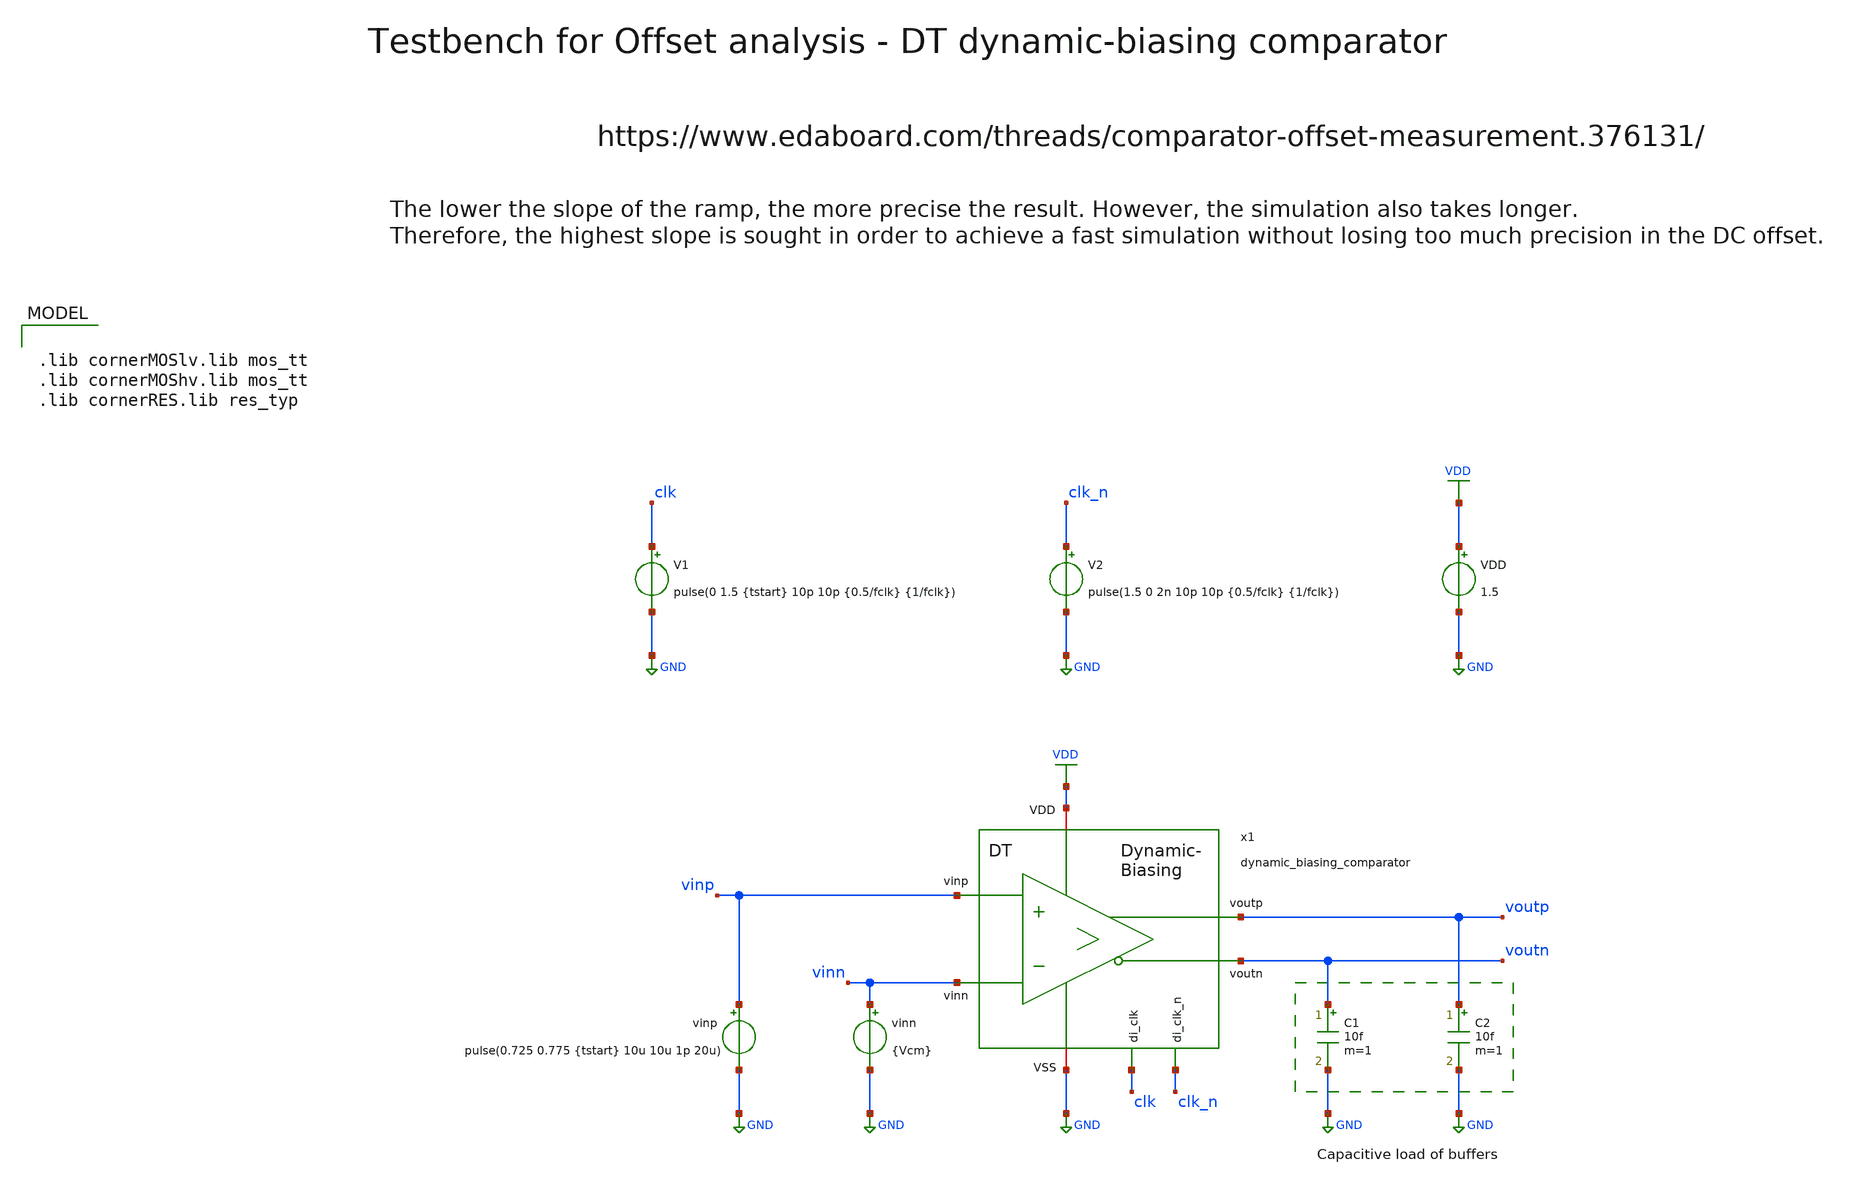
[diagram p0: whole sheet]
** sch_path: SG13G2_ATBS-ADC-main/xschem/comparator/discrete_time/Dynamic-biasing/testbenches/dynamic_biasing_comparator_tb_tran_offset.sch
**.subckt dynamic_biasing_comparator_tb_tran_offset
VDD VDD GND 1.5
V1 clk GND pulse(0 1.5 {tstart} 10p 10p {0.5/fclk} {1/fclk})
vinn vinn GND {Vcm}
vinp vinp GND pulse(0.725 0.775 {tstart} 10u 10u 1p 20u)
V2 clk_n GND pulse(1.5 0 2n 10p 10p {0.5/fclk} {1/fclk})
C1 voutn GND 10f m=1
C2 voutp GND 10f m=1
x1 clk_n clk VDD voutp vinp GND voutn vinn dynamic_biasing_comparator
**** begin user architecture code

.lib cornerMOSlv.lib mos_tt
.lib cornerMOShv.lib mos_tt
.lib cornerRES.lib res_typ



.param temp=27
.param fclk=8000000
.param tstart=2n
.param Vcm=0.75
.csparam fclk=fclk
.csparam tstart=tstart
.csparam Vcm=Vcm
.options klu method=gear reltol=1e-3 abstol=1e-12 gmin=1e-15
.control
* save all

* User Constants
let tstop = 20u
let tstep = 1/fclk

* Operating Point Analysis
op
remzerovec
write dynamic_biasing_comparator_tb_tran_offset.raw
set appendwrite

* Transient Analysis
tran $&tstep $&tstop
write dynamic_biasing_comparator_tb_tran_offset.raw

* Measure offset increasing ramp
let voutp_limit = 0.9 * 1.5
meas tran tcross WHEN v(voutp)=voutp_limit RISE=1
print tcross
meas tran vinp_voff FIND v(vinp) at=tcross
let voff_inc = vinp_voff - Vcm
print voff_inc

* Measure offset decreasing ramp
let voutn_limit = 0.9 * 1.5
let tmiddle = tstop/2
meas tran tcross WHEN v(voutn)=voutn_limit from=tmiddle RISE=1
print tcross
meas tran vinp_voff FIND v(vinp) at=tcross
let voff_dec = vinp_voff - Vcm
print voff_dec

* Plotting
plot v(clk) v(voutp) v(voutn) v(vinp) v(vinn)

* Writing Data
set wr_singlescale
set wr_vecnames
wrdata
+ /foss/designs/SG13G2_ATBS-ADC-main/python/plot_simulations/data/dynamic_biasing_comparator_tb_tran_offset.txt v(clk) v(voutp) v(voutn) v(vinp) v(vinn)

*quit
.endc

**** end user architecture code
**.ends

* expanding   symbol:  comparator/discrete_time/Dynamic-biasing/dynamic_biasing_comparator.sym # of
*+ pins=8
** sym_path: SG13G2_ATBS-ADC-main/xschem/comparator/discrete_time/Dynamic-biasing/dynamic_biasing_comparator.sym
** sch_path: SG13G2_ATBS-ADC-main/xschem/comparator/discrete_time/Dynamic-biasing/dynamic_biasing_comparator.sch
.subckt dynamic_biasing_comparator di_clk_n di_clk VDD voutp vinp VSS voutn vinn
*.iopin VDD
*.opin voutp
*.opin voutn
*.ipin di_clk_n
*.iopin VSS
*.ipin vinp
*.ipin vinn
*.ipin di_clk
XM3a vs di_clk vctail VSS sg13_lv_nmos w=1.0u l=0.13u ng=1 m=1 mm_ok=1
XM12 voutp di_clk_n VSS VSS sg13_lv_nmos w=1.0u l=0.13u ng=1 m=1 mm_ok=1
XM8 net1 voutn VDD VDD sg13_lv_pmos w=2.0u l=0.13u ng=2 m=1 mm_ok=1
XM10 voutp voutn VSS VSS sg13_lv_nmos w=1.0u l=0.13u ng=1 m=1 mm_ok=1
XM11 voutn voutp VSS VSS sg13_lv_nmos w=1.0u l=0.13u ng=1 m=1 mm_ok=1
XM13 voutn di_clk_n VSS VSS sg13_lv_nmos w=1.0u l=0.13u ng=1 m=1 mm_ok=1
CPn vcpn VSS 300f m=1
CPp vcpp VSS 300f m=1
XM9 net2 voutp VDD VDD sg13_lv_pmos w=2.0u l=0.13u ng=2 m=1 mm_ok=1
XM6 voutp vcpn net1 VDD sg13_lv_pmos w=2.0u l=0.13u ng=2 m=1 mm_ok=1
XM7 voutn vcpp net2 VDD sg13_lv_pmos w=2.0u l=0.13u ng=2 m=1 mm_ok=1
CTAIL vctail VSS 600f m=1
XM3b vctail di_clk_n VSS VSS sg13_lv_nmos w=1.0u l=0.13u ng=1 m=1 mm_ok=1
XM1 vcpn vinp vs VSS sg13_lv_nmos w=1.0u l=0.13u ng=1 m=1 mm_ok=1
XM2 vcpp vinn vs VSS sg13_lv_nmos w=1.0u l=0.13u ng=1 m=1 mm_ok=1
XM4 vcpn di_clk VDD VDD sg13_lv_pmos w=1.0u l=0.13u ng=1 m=1 mm_ok=1
XM5 vcpp di_clk VDD VDD sg13_lv_pmos w=1.0u l=0.13u ng=1 m=1 mm_ok=1
.ends

.GLOBAL GND
.GLOBAL VDD
.end
